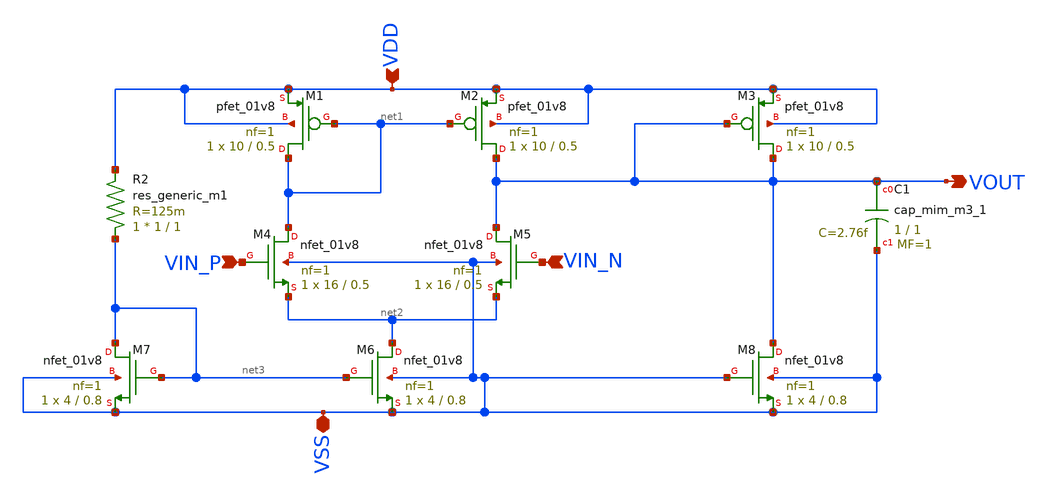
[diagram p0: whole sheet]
** sch_path: analog/schematics/bootcamp_opamp.sch
**.subckt bootcamp_opamp VIN_P VIN_N VSS VOUT VDD
*.ipin VIN_P
*.ipin VIN_N
*.iopin VSS
*.opin VOUT
*.ipin VDD
XM1 net1 net1 VDD VDD sky130_fd_pr__pfet_01v8 L=0.5 W=10 nf=1 ad='int((nf+1)/2) * W/nf * 0.29' as='int((nf+2)/2) * W/nf * 0.29'
+ pd='2*int((nf+1)/2) * (W/nf + 0.29)' ps='2*int((nf+2)/2) * (W/nf + 0.29)' nrd='0.29 / W' nrs='0.29 / W'
+ sa=0 sb=0 sd=0 mult=1 m=1
XM2 VOUT net1 VDD VDD sky130_fd_pr__pfet_01v8 L=0.5 W=10 nf=1 ad='int((nf+1)/2) * W/nf * 0.29' as='int((nf+2)/2) * W/nf * 0.29'
+ pd='2*int((nf+1)/2) * (W/nf + 0.29)' ps='2*int((nf+2)/2) * (W/nf + 0.29)' nrd='0.29 / W' nrs='0.29 / W'
+ sa=0 sb=0 sd=0 mult=1 m=1
XM3 VOUT VOUT VDD VDD sky130_fd_pr__pfet_01v8 L=0.5 W=10 nf=1 ad='int((nf+1)/2) * W/nf * 0.29' as='int((nf+2)/2) * W/nf * 0.29'
+ pd='2*int((nf+1)/2) * (W/nf + 0.29)' ps='2*int((nf+2)/2) * (W/nf + 0.29)' nrd='0.29 / W' nrs='0.29 / W'
+ sa=0 sb=0 sd=0 mult=1 m=1
XM4 net1 VIN_P net2 VSS sky130_fd_pr__nfet_01v8 L=0.5 W=16 nf=1 ad='int((nf+1)/2) * W/nf * 0.29' as='int((nf+2)/2) * W/nf * 0.29'
+ pd='2*int((nf+1)/2) * (W/nf + 0.29)' ps='2*int((nf+2)/2) * (W/nf + 0.29)' nrd='0.29 / W' nrs='0.29 / W'
+ sa=0 sb=0 sd=0 mult=1 m=1
XM5 VOUT VIN_N net2 VSS sky130_fd_pr__nfet_01v8 L=0.5 W=16 nf=1 ad='int((nf+1)/2) * W/nf * 0.29' as='int((nf+2)/2) * W/nf * 0.29'
+ pd='2*int((nf+1)/2) * (W/nf + 0.29)' ps='2*int((nf+2)/2) * (W/nf + 0.29)' nrd='0.29 / W' nrs='0.29 / W'
+ sa=0 sb=0 sd=0 mult=1 m=1
XM6 net2 net3 VSS VSS sky130_fd_pr__nfet_01v8 L=0.8 W=4 nf=1 ad='int((nf+1)/2) * W/nf * 0.29' as='int((nf+2)/2) * W/nf * 0.29'
+ pd='2*int((nf+1)/2) * (W/nf + 0.29)' ps='2*int((nf+2)/2) * (W/nf + 0.29)' nrd='0.29 / W' nrs='0.29 / W'
+ sa=0 sb=0 sd=0 mult=1 m=1
XM7 net3 net3 VSS VSS sky130_fd_pr__nfet_01v8 L=0.8 W=4 nf=1 ad='int((nf+1)/2) * W/nf * 0.29' as='int((nf+2)/2) * W/nf * 0.29'
+ pd='2*int((nf+1)/2) * (W/nf + 0.29)' ps='2*int((nf+2)/2) * (W/nf + 0.29)' nrd='0.29 / W' nrs='0.29 / W'
+ sa=0 sb=0 sd=0 mult=1 m=1
XM8 VOUT VSS VSS VSS sky130_fd_pr__nfet_01v8 L=0.8 W=4 nf=1 ad='int((nf+1)/2) * W/nf * 0.29' as='int((nf+2)/2) * W/nf * 0.29'
+ pd='2*int((nf+1)/2) * (W/nf + 0.29)' ps='2*int((nf+2)/2) * (W/nf + 0.29)' nrd='0.29 / W' nrs='0.29 / W'
+ sa=0 sb=0 sd=0 mult=1 m=1
XC1 VOUT VSS sky130_fd_pr__cap_mim_m3_1 W=1 L=1 MF=1 m=1
R2 net3 VDD sky130_fd_pr__res_generic_m1 W=1 L=1 m=1
**.ends
.end
